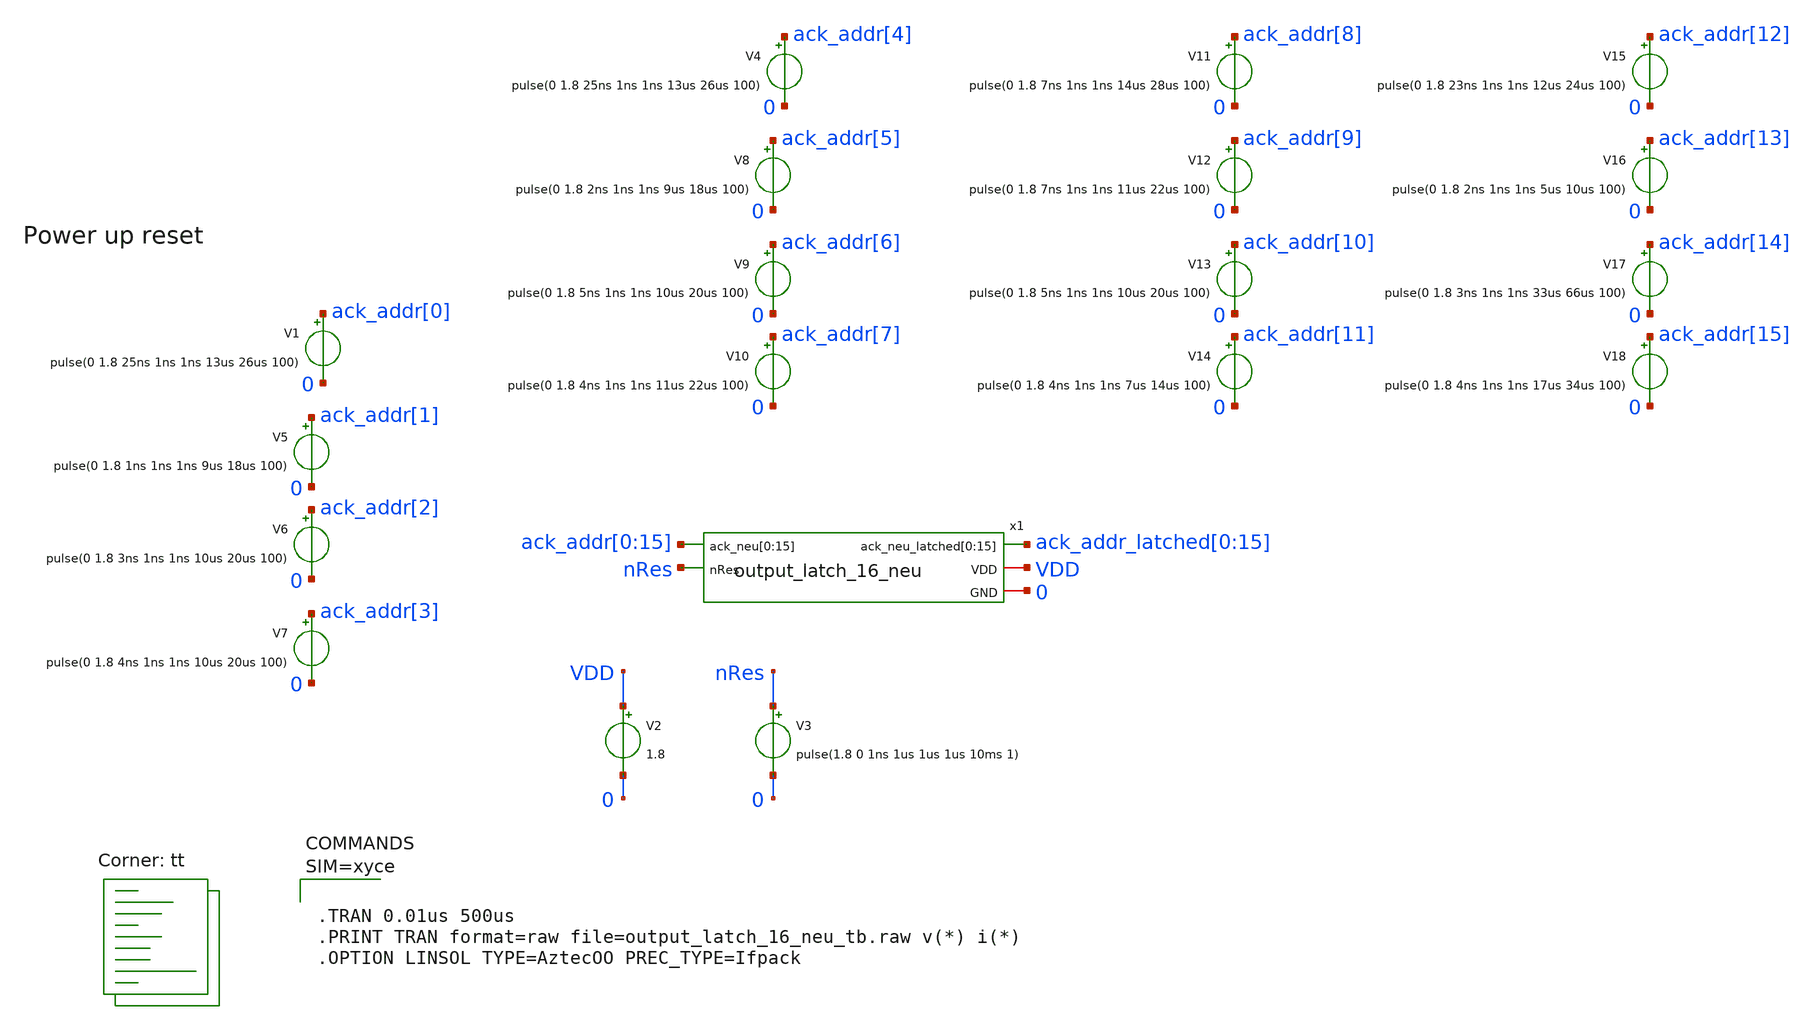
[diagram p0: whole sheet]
** sch_path: design/xschem/output_latch_16_neu_tb.sch
**.subckt output_latch_16_neu_tb
V3 nRes 0 pulse(1.8 0 1ns 1us 1us 1us 10ms 1)
V1 ack_addr[0] 0 pulse(0 1.8 25ns 1ns 1ns 13us 26us 100)
V5 ack_addr[1] 0 pulse(0 1.8 1ns 1ns 1ns 9us 18us 100)
V6 ack_addr[2] 0 pulse(0 1.8 3ns 1ns 1ns 10us 20us 100)
V7 ack_addr[3] 0 pulse(0 1.8 4ns 1ns 1ns 10us 20us 100)
V2 VDD 0 1.8
x1 ack_addr_latched[0] ack_addr_latched[1] ack_addr_latched[2] ack_addr_latched[3]
+ ack_addr_latched[4] ack_addr_latched[5] ack_addr_latched[6] ack_addr_latched[7] ack_addr_latched[8] ack_addr_latched[9]
+ ack_addr_latched[10] ack_addr_latched[11] ack_addr_latched[12] ack_addr_latched[13] ack_addr_latched[14]
+ ack_addr_latched[15] ack_addr[0] ack_addr[1] ack_addr[2] ack_addr[3] ack_addr[4] ack_addr[5] ack_addr[6] ack_addr[7]
+ ack_addr[8] ack_addr[9] ack_addr[10] ack_addr[11] ack_addr[12] ack_addr[13] ack_addr[14] ack_addr[15] nRes VDD
+ 0 output_latch_16_neu
V4 ack_addr[4] 0 pulse(0 1.8 25ns 1ns 1ns 13us 26us 100)
V8 ack_addr[5] 0 pulse(0 1.8 2ns 1ns 1ns 9us 18us 100)
V9 ack_addr[6] 0 pulse(0 1.8 5ns 1ns 1ns 10us 20us 100)
V10 ack_addr[7] 0 pulse(0 1.8 4ns 1ns 1ns 11us 22us 100)
V11 ack_addr[8] 0 pulse(0 1.8 7ns 1ns 1ns 14us 28us 100)
V12 ack_addr[9] 0 pulse(0 1.8 7ns 1ns 1ns 11us 22us 100)
V13 ack_addr[10] 0 pulse(0 1.8 5ns 1ns 1ns 10us 20us 100)
V14 ack_addr[11] 0 pulse(0 1.8 4ns 1ns 1ns 7us 14us 100)
V15 ack_addr[12] 0 pulse(0 1.8 23ns 1ns 1ns 12us 24us 100)
V16 ack_addr[13] 0 pulse(0 1.8 2ns 1ns 1ns 5us 10us 100)
V17 ack_addr[14] 0 pulse(0 1.8 3ns 1ns 1ns 33us 66us 100)
V18 ack_addr[15] 0 pulse(0 1.8 4ns 1ns 1ns 17us 34us 100)
**** begin user architecture code


* Standard cell simulation files
.include $::SKYWATER_STDCELLS/sky130_fd_sc_hd.spice


.lib $::SKYWATER_MODELS/sky130.lib.spice tt



**** end user architecture code
**.ends

* expanding   symbol:  output_latch_16_neu.sym # of pins=5
** sym_path: design/xschem/output_latch_16_neu.sym
** sch_path: design/xschem/output_latch_16_neu.sch
.subckt output_latch_16_neu ack_neu_latched[0] ack_neu_latched[1] ack_neu_latched[2]
+ ack_neu_latched[3] ack_neu_latched[4] ack_neu_latched[5] ack_neu_latched[6] ack_neu_latched[7] ack_neu_latched[8]
+ ack_neu_latched[9] ack_neu_latched[10] ack_neu_latched[11] ack_neu_latched[12] ack_neu_latched[13] ack_neu_latched[14]
+ ack_neu_latched[15] ack_neu[0] ack_neu[1] ack_neu[2] ack_neu[3] ack_neu[4] ack_neu[5] ack_neu[6] ack_neu[7] ack_neu[8]
+ ack_neu[9] ack_neu[10] ack_neu[11] ack_neu[12] ack_neu[13] ack_neu[14] ack_neu[15] nRes VDD GND
*.ipin
*+ ack_neu[0],ack_neu[1],ack_neu[2],ack_neu[3],ack_neu[4],ack_neu[5],ack_neu[6],ack_neu[7],ack_neu[8],ack_neu[9],ack_neu[10],ack_neu[11],ack_neu[12],ack_neu[13],ack_neu[14],ack_neu[15]
*.ipin nRes
*.opin
*+ ack_neu_latched[0],ack_neu_latched[1],ack_neu_latched[2],ack_neu_latched[3],ack_neu_latched[4],ack_neu_latched[5],ack_neu_latched[6],ack_neu_latched[7],ack_neu_latched[8],ack_neu_latched[9],ack_neu_latched[10],ack_neu_latched[11],ack_neu_latched[12],ack_neu_latched[13],ack_neu_latched[14],ack_neu_latched[15]
*.iopin VDD
*.iopin GND
x2[0] latchAddr ack_neu[0] nRes GND GND VDD VDD ack_neu_latched[0] sky130_fd_sc_hd__dfrtp_1
x2[1] latchAddr ack_neu[1] nRes GND GND VDD VDD ack_neu_latched[1] sky130_fd_sc_hd__dfrtp_1
x2[2] latchAddr ack_neu[2] nRes GND GND VDD VDD ack_neu_latched[2] sky130_fd_sc_hd__dfrtp_1
x2[3] latchAddr ack_neu[3] nRes GND GND VDD VDD ack_neu_latched[3] sky130_fd_sc_hd__dfrtp_1
x2[4] latchAddr ack_neu[4] nRes GND GND VDD VDD ack_neu_latched[4] sky130_fd_sc_hd__dfrtp_1
x2[5] latchAddr ack_neu[5] nRes GND GND VDD VDD ack_neu_latched[5] sky130_fd_sc_hd__dfrtp_1
x2[6] latchAddr ack_neu[6] nRes GND GND VDD VDD ack_neu_latched[6] sky130_fd_sc_hd__dfrtp_1
x2[7] latchAddr ack_neu[7] nRes GND GND VDD VDD ack_neu_latched[7] sky130_fd_sc_hd__dfrtp_1
x2[8] latchAddr ack_neu[8] nRes GND GND VDD VDD ack_neu_latched[8] sky130_fd_sc_hd__dfrtp_1
x2[9] latchAddr ack_neu[9] nRes GND GND VDD VDD ack_neu_latched[9] sky130_fd_sc_hd__dfrtp_1
x2[10] latchAddr ack_neu[10] nRes GND GND VDD VDD ack_neu_latched[10] sky130_fd_sc_hd__dfrtp_1
x2[11] latchAddr ack_neu[11] nRes GND GND VDD VDD ack_neu_latched[11] sky130_fd_sc_hd__dfrtp_1
x2[12] latchAddr ack_neu[12] nRes GND GND VDD VDD ack_neu_latched[12] sky130_fd_sc_hd__dfrtp_1
x2[13] latchAddr ack_neu[13] nRes GND GND VDD VDD ack_neu_latched[13] sky130_fd_sc_hd__dfrtp_1
x2[14] latchAddr ack_neu[14] nRes GND GND VDD VDD ack_neu_latched[14] sky130_fd_sc_hd__dfrtp_1
x2[15] latchAddr ack_neu[15] nRes GND GND VDD VDD ack_neu_latched[15] sky130_fd_sc_hd__dfrtp_1
x3 ack_neu[0] ack_neu[1] ack_neu[2] ack_neu[3] net2 ack_neu[4] ack_neu[5] ack_neu[6] ack_neu[7] VDD
+ GND or8
x1 ack_neu[8] ack_neu[9] ack_neu[10] ack_neu[11] net1 ack_neu[12] ack_neu[13] ack_neu[14]
+ ack_neu[15] VDD GND or8
x2 net2 net1 GND GND VDD VDD latchAddr sky130_fd_sc_hd__or2_1
.ends


* expanding   symbol:  or8.sym # of pins=11
** sym_path: design/xschem/or8.sym
** sch_path: design/xschem/or8.sch
.subckt or8 h g f e out d c b a VDD GND
*.ipin a
*.ipin b
*.ipin c
*.ipin d
*.ipin e
*.ipin f
*.ipin g
*.ipin h
*.opin out
*.iopin VDD
*.iopin GND
x1 h g f e GND GND VDD VDD net1 sky130_fd_sc_hd__or4_1
x2 d c b a GND GND VDD VDD net2 sky130_fd_sc_hd__or4_1
x3 net1 net2 GND GND VDD VDD out sky130_fd_sc_hd__or2_1
.ends

.end
